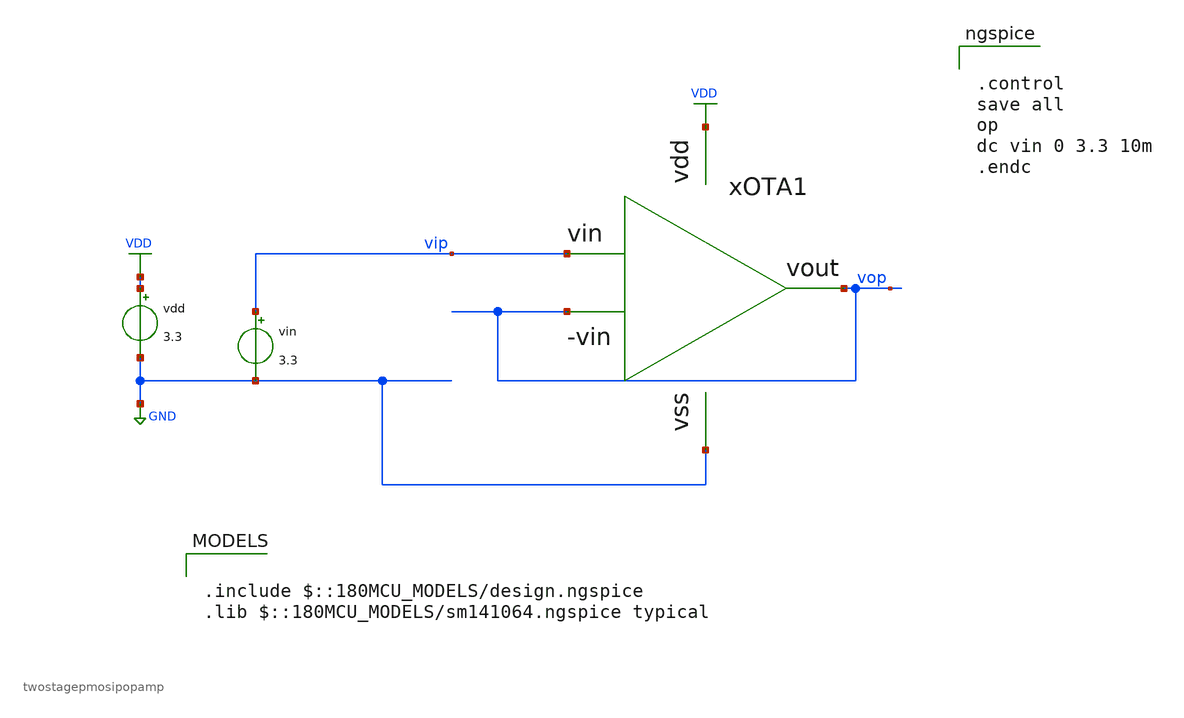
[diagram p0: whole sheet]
** sch_path: designs/OTA_pmosfinal_tb.sch
**.subckt OTA_pmosfinal_tb
vin vip GND 3.3
vdd VDD GND 3.3
xOTA1 vip VDD vop vop GND twostagepmosipopamp
**** begin user architecture code

.include $::180MCU_MODELS/design.ngspice
.lib $::180MCU_MODELS/sm141064.ngspice typical



.control
save all
op
dc vin 0 3.3 10m
.endc

**** end user architecture code
**.ends
.GLOBAL GND
.GLOBAL VDD
.end
